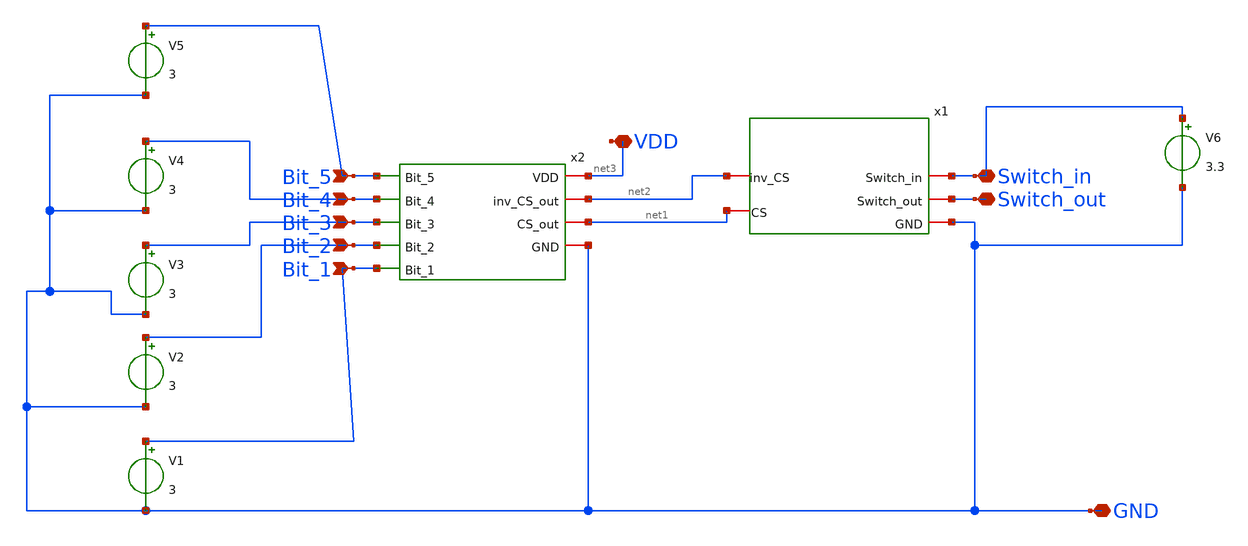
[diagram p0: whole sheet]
** sch_path: ProjectDesigns/Switch_and_5BITAND/Sim_Switch_and_5Bit_AND.sch
**.subckt Sim_Switch_and_5Bit_AND Bit_5 Bit_4 Bit_3 Bit_2 Bit_1 Switch_in Switch_out GND VDD
*.ipin Bit_5
*.ipin Bit_4
*.ipin Bit_3
*.ipin Bit_2
*.ipin Bit_1
*.iopin Switch_in
*.iopin Switch_out
*.iopin GND
*.iopin VDD
V1 Bit_1 GND 3
V2 Bit_2 GND 3
V3 Bit_3 GND 3
V4 Bit_4 GND 3
V5 Bit_5 GND 3
V6 Switch_in GND 3.3
x1 net2 net1 Switch_in Switch_out GND Switch
x2 net3 net2 Bit_5 Bit_4 net1 Bit_3 Bit_2 Bit_1 GND 5bit_AND
**.ends

* expanding   symbol:  /home/shalini1234/Project/Switch.sym # of pins=5
** sym_path: ProjectDesigns/Switch/Switch.sym
** sch_path: ProjectDesigns/Switch/Switch.sch
.subckt Switch inv_CS CS Switch_in Switch_out GND
*.iopin Switch_in
*.iopin Switch_out
*.iopin CS
*.iopin inv_CS
*.iopin GND
XM1 Switch_in CS Switch_out Switch_out sky130_fd_pr__nfet_01v8 L=0.15 W=1 nf=1 ad='int((nf+1)/2) * W/nf * 0.29'
+ as='int((nf+2)/2) * W/nf * 0.29' pd='2*int((nf+1)/2) * (W/nf + 0.29)' ps='2*int((nf+2)/2) * (W/nf + 0.29)'
+ nrd='0.29 / W' nrs='0.29 / W' sa=0 sb=0 sd=0 mult=1 m=1
XM2 Switch_out inv_CS Switch_in Switch_in sky130_fd_pr__pfet_01v8 L=0.15 W=1 nf=1 ad='int((nf+1)/2) * W/nf * 0.29'
+ as='int((nf+2)/2) * W/nf * 0.29' pd='2*int((nf+1)/2) * (W/nf + 0.29)' ps='2*int((nf+2)/2) * (W/nf + 0.29)'
+ nrd='0.29 / W' nrs='0.29 / W' sa=0 sb=0 sd=0 mult=1 m=1
XM5 Switch_out inv_CS GND GND sky130_fd_pr__nfet_01v8 L=0.15 W=1 nf=1 ad='int((nf+1)/2) * W/nf * 0.29'
+ as='int((nf+2)/2) * W/nf * 0.29' pd='2*int((nf+1)/2) * (W/nf + 0.29)' ps='2*int((nf+2)/2) * (W/nf + 0.29)'
+ nrd='0.29 / W' nrs='0.29 / W' sa=0 sb=0 sd=0 mult=1 m=1
.ends


* expanding   symbol:  /home/shalini1234/Project/5bit_AND.sym # of pins=9
** sym_path: ProjectDesigns/5BitAND/5bit_AND.sym
** sch_path: ProjectDesigns/5BitAND/5bit_AND.sch
.subckt 5bit_AND VDD inv_CS_out Bit_5 Bit_4 CS_out Bit_3 Bit_2 Bit_1 GND
*.ipin Bit_1
*.ipin Bit_3
*.ipin Bit_2
*.ipin Bit_4
*.ipin Bit_5
*.iopin inv_CS_out
*.iopin CS_out
*.iopin VDD
*.iopin GND
XM1 inv_CS_out Bit_5 net1 net1 sky130_fd_pr__nfet_01v8 L=0.15 W=1 nf=1 ad='int((nf+1)/2) * W/nf * 0.29'
+ as='int((nf+2)/2) * W/nf * 0.29' pd='2*int((nf+1)/2) * (W/nf + 0.29)' ps='2*int((nf+2)/2) * (W/nf + 0.29)'
+ nrd='0.29 / W' nrs='0.29 / W' sa=0 sb=0 sd=0 mult=1 m=1
XM2 net1 Bit_4 net2 net2 sky130_fd_pr__nfet_01v8 L=0.15 W=1 nf=1 ad='int((nf+1)/2) * W/nf * 0.29' as='int((nf+2)/2) * W/nf * 0.29'
+ pd='2*int((nf+1)/2) * (W/nf + 0.29)' ps='2*int((nf+2)/2) * (W/nf + 0.29)' nrd='0.29 / W' nrs='0.29 / W'
+ sa=0 sb=0 sd=0 mult=1 m=1
XM3 net2 Bit_3 net3 net3 sky130_fd_pr__nfet_01v8 L=0.15 W=1 nf=1 ad='int((nf+1)/2) * W/nf * 0.29' as='int((nf+2)/2) * W/nf * 0.29'
+ pd='2*int((nf+1)/2) * (W/nf + 0.29)' ps='2*int((nf+2)/2) * (W/nf + 0.29)' nrd='0.29 / W' nrs='0.29 / W'
+ sa=0 sb=0 sd=0 mult=1 m=1
XM4 net3 Bit_2 net4 net4 sky130_fd_pr__nfet_01v8 L=0.15 W=1 nf=1 ad='int((nf+1)/2) * W/nf * 0.29' as='int((nf+2)/2) * W/nf * 0.29'
+ pd='2*int((nf+1)/2) * (W/nf + 0.29)' ps='2*int((nf+2)/2) * (W/nf + 0.29)' nrd='0.29 / W' nrs='0.29 / W'
+ sa=0 sb=0 sd=0 mult=1 m=1
XM5 net4 Bit_1 GND GND sky130_fd_pr__nfet_01v8 L=0.15 W=1 nf=1 ad='int((nf+1)/2) * W/nf * 0.29' as='int((nf+2)/2) * W/nf * 0.29'
+ pd='2*int((nf+1)/2) * (W/nf + 0.29)' ps='2*int((nf+2)/2) * (W/nf + 0.29)' nrd='0.29 / W' nrs='0.29 / W'
+ sa=0 sb=0 sd=0 mult=1 m=1
XM6 inv_CS_out Bit_3 VDD VDD sky130_fd_pr__pfet_01v8 L=0.15 W=1 nf=1 ad='int((nf+1)/2) * W/nf * 0.29'
+ as='int((nf+2)/2) * W/nf * 0.29' pd='2*int((nf+1)/2) * (W/nf + 0.29)' ps='2*int((nf+2)/2) * (W/nf + 0.29)'
+ nrd='0.29 / W' nrs='0.29 / W' sa=0 sb=0 sd=0 mult=1 m=1
XM7 inv_CS_out Bit_2 VDD VDD sky130_fd_pr__pfet_01v8 L=0.15 W=1 nf=1 ad='int((nf+1)/2) * W/nf * 0.29'
+ as='int((nf+2)/2) * W/nf * 0.29' pd='2*int((nf+1)/2) * (W/nf + 0.29)' ps='2*int((nf+2)/2) * (W/nf + 0.29)'
+ nrd='0.29 / W' nrs='0.29 / W' sa=0 sb=0 sd=0 mult=1 m=1
XM8 inv_CS_out Bit_1 VDD VDD sky130_fd_pr__pfet_01v8 L=0.15 W=1 nf=1 ad='int((nf+1)/2) * W/nf * 0.29'
+ as='int((nf+2)/2) * W/nf * 0.29' pd='2*int((nf+1)/2) * (W/nf + 0.29)' ps='2*int((nf+2)/2) * (W/nf + 0.29)'
+ nrd='0.29 / W' nrs='0.29 / W' sa=0 sb=0 sd=0 mult=1 m=1
XM9 inv_CS_out Bit_4 VDD VDD sky130_fd_pr__pfet_01v8 L=0.15 W=1 nf=1 ad='int((nf+1)/2) * W/nf * 0.29'
+ as='int((nf+2)/2) * W/nf * 0.29' pd='2*int((nf+1)/2) * (W/nf + 0.29)' ps='2*int((nf+2)/2) * (W/nf + 0.29)'
+ nrd='0.29 / W' nrs='0.29 / W' sa=0 sb=0 sd=0 mult=1 m=1
XM10 inv_CS_out Bit_5 VDD VDD sky130_fd_pr__pfet_01v8 L=0.15 W=1 nf=1 ad='int((nf+1)/2) * W/nf * 0.29'
+ as='int((nf+2)/2) * W/nf * 0.29' pd='2*int((nf+1)/2) * (W/nf + 0.29)' ps='2*int((nf+2)/2) * (W/nf + 0.29)'
+ nrd='0.29 / W' nrs='0.29 / W' sa=0 sb=0 sd=0 mult=1 m=1
XM11 CS_out inv_CS_out GND GND sky130_fd_pr__nfet_01v8 L=0.15 W=1 nf=1 ad='int((nf+1)/2) * W/nf * 0.29'
+ as='int((nf+2)/2) * W/nf * 0.29' pd='2*int((nf+1)/2) * (W/nf + 0.29)' ps='2*int((nf+2)/2) * (W/nf + 0.29)'
+ nrd='0.29 / W' nrs='0.29 / W' sa=0 sb=0 sd=0 mult=1 m=1
XM12 CS_out inv_CS_out VDD VDD sky130_fd_pr__pfet_01v8 L=0.15 W=1 nf=1 ad='int((nf+1)/2) * W/nf * 0.29'
+ as='int((nf+2)/2) * W/nf * 0.29' pd='2*int((nf+1)/2) * (W/nf + 0.29)' ps='2*int((nf+2)/2) * (W/nf + 0.29)'
+ nrd='0.29 / W' nrs='0.29 / W' sa=0 sb=0 sd=0 mult=1 m=1
.ends

.end
